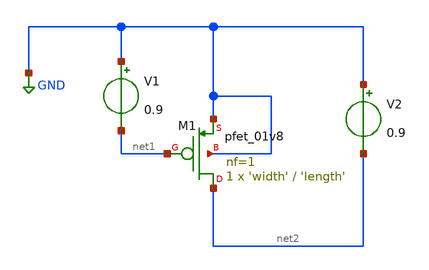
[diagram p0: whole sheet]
** sch_path: PMOS_Charac/pmos_gmid.sch
**.subckt pmos_gmid
XM1 net2 net1 GND GND sky130_fd_pr__pfet_01v8 L='length' W='width' nf=1 ad='int((nf+1)/2) * W/nf * 0.29'
+ as='int((nf+2)/2) * W/nf * 0.29' pd='2*int((nf+1)/2) * (W/nf + 0.29)' ps='2*int((nf+2)/2) * (W/nf + 0.29)'
+ nrd='0.29 / W' nrs='0.29 / W' sa=0 sb=0 sd=0 mult=1 m=1
V1 GND net1 0.9
V2 GND net2 0.9
**** begin user architecture code



.include init.txt
.include pmos_params.txt

.param length = 0.3
.param width = 1






**** end user architecture code
**.ends
.GLOBAL GND
.end
